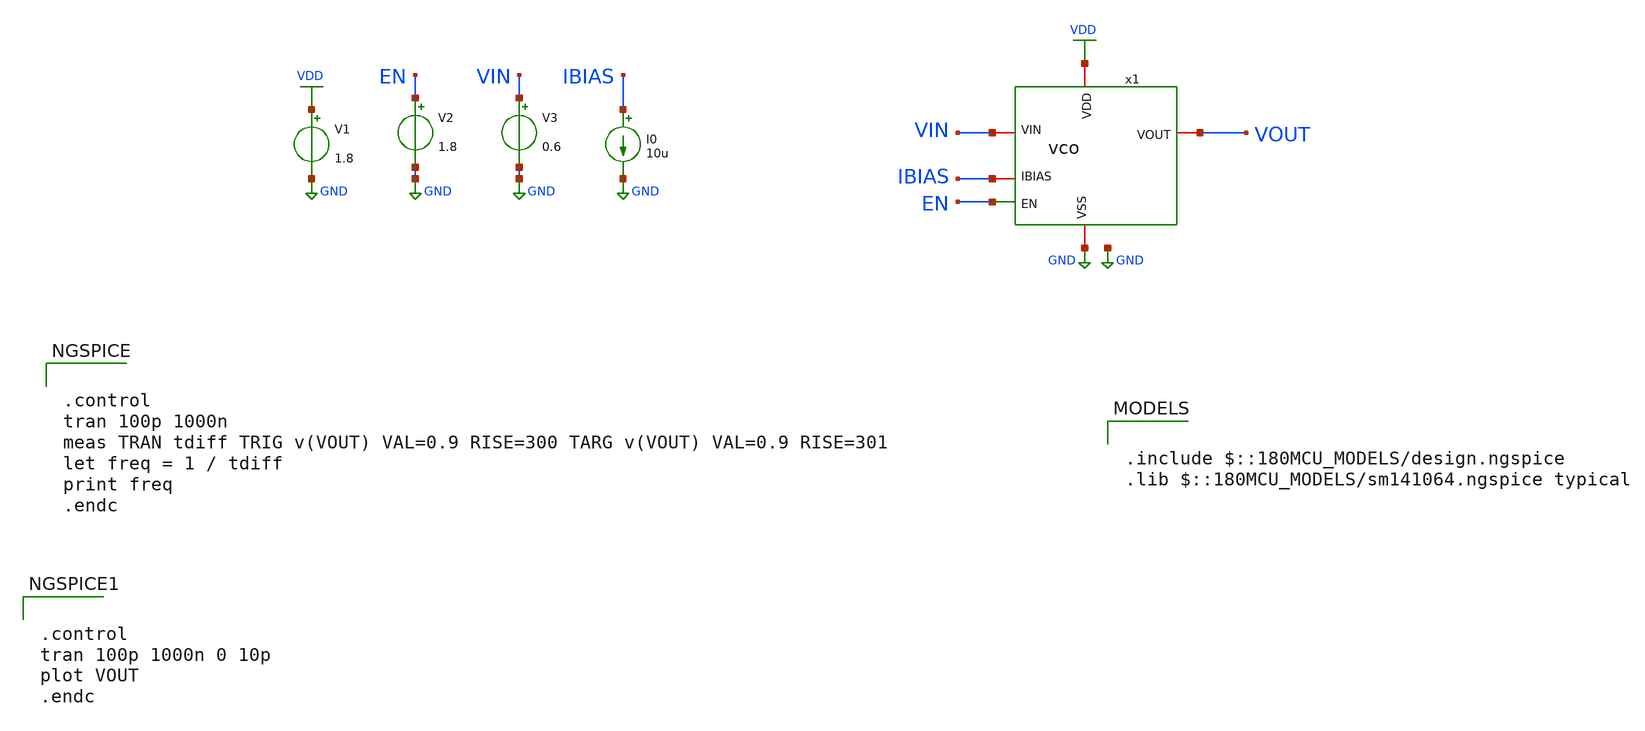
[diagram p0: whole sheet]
** sch_path: designs/libs/tb_vco/tb_vco/tb_vco.sch
**.subckt tb_vco
V1 VDD GND 1.8
V3 VIN GND 0.6
I0 IBIAS GND 10u
V2 EN GND 1.8
x1 VDD IBIAS VOUT EN GND VIN vco
**** begin user architecture code

.include $::180MCU_MODELS/design.ngspice
.lib $::180MCU_MODELS/sm141064.ngspice typical



.control
tran 100p 1000n
meas TRAN tdiff TRIG v(VOUT) VAL=0.9 RISE=300 TARG v(VOUT) VAL=0.9 RISE=301
let freq = 1 / tdiff
print freq
.endc




.control
tran 100p 1000n 0 10p
plot VOUT
.endc


**** end user architecture code
**.ends
.GLOBAL GND
.GLOBAL VDD
.end
